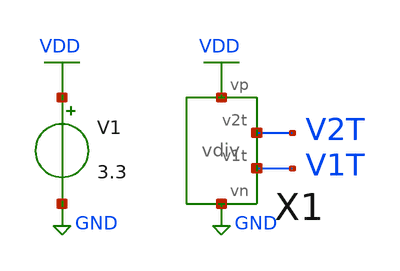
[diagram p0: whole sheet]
** sch_path: xschem/vdiv_tb.sch
**.subckt vdiv_tb
X1 V1T V2T VDD GND vdiv
V1 VDD GND 3.3
.save i(v1)
**** begin user architecture code


.option wnflag=1
.lib /usr/local/share/pdk/sky130A/libs.tech/ngspice/sky130.lib.spice tt
.op
.save all


**** end user architecture code
**.ends

* expanding   symbol:  vdiv.sym # of pins=4
** sym_path: xschem/vdiv.sym
** sch_path: xschem/vdiv.sch
.subckt vdiv v1t v2t vp vn
*.iopin vp
*.iopin v2t
*.iopin v1t
*.iopin vn
XR1 v2t vp vn res100k
XR2 v1t v2t vn res100k
XR3 vn v1t vn res100k
.ends


* expanding   symbol:  res100k.sym # of pins=3
** sym_path: xschem/res100k.sym
** sch_path: xschem/res100k.sch
.subckt res100k bot top sub
*.iopin top
*.iopin bot
*.iopin sub
XR1 net1 top sub sky130_fd_pr__res_xhigh_po W=0.35 L=3.5 mult=1 m=1
XR2 net2 net1 sub sky130_fd_pr__res_xhigh_po W=0.35 L=3.5 mult=1 m=1
XR3 net3 net2 sub sky130_fd_pr__res_xhigh_po W=0.35 L=3.5 mult=1 m=1
XR4 net4 net3 sub sky130_fd_pr__res_xhigh_po W=0.35 L=3.5 mult=1 m=1
XR5 bot net4 sub sky130_fd_pr__res_xhigh_po W=0.35 L=3.5 mult=1 m=1
.ends

.GLOBAL GND
.GLOBAL VDD
.end
